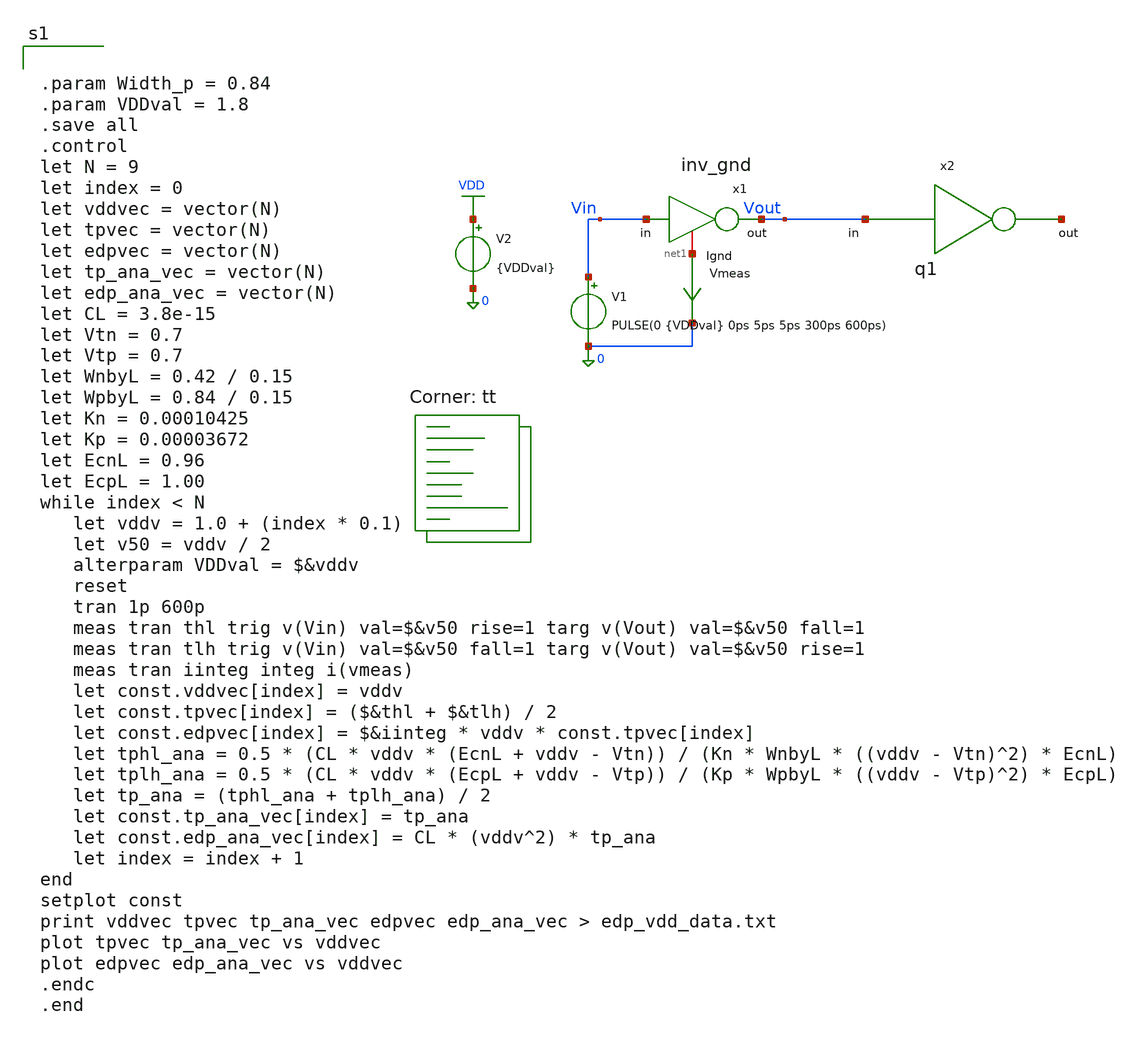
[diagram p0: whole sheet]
** sch_path: tutorial-3/source/qn_1_b.sch
**.subckt qn_1_b
V1 Vin 0 PULSE(0 {VDDval} 0ps 5ps 5ps 300ps 600ps)
V2 VDD 0 {VDDval}
x1 Vout Vin net1 inv_gnd
Vmeas net1 0 0
.save i(vmeas)
x2 net2 Vout q1
**** begin user architecture code


.param Width_p = 0.84
.param VDDval = 1.8
.save all
.control
let N = 9
let index = 0
let vddvec = vector(N)
let tpvec = vector(N)
let edpvec = vector(N)
let tp_ana_vec = vector(N)
let edp_ana_vec = vector(N)
let CL = 3.8e-15
let Vtn = 0.7
let Vtp = 0.7
let WnbyL = 0.42 / 0.15
let WpbyL = 0.84 / 0.15
let Kn = 0.00010425
let Kp = 0.00003672
let EcnL = 0.96
let EcpL = 1.00
while index < N
   let vddv = 1.0 + (index * 0.1)
   let v50 = vddv / 2
   alterparam VDDval = $&vddv
   reset
   tran 1p 600p
   meas tran thl trig v(Vin) val=$&v50 rise=1 targ v(Vout) val=$&v50 fall=1
   meas tran tlh trig v(Vin) val=$&v50 fall=1 targ v(Vout) val=$&v50 rise=1
   meas tran iinteg integ i(vmeas)
   let const.vddvec[index] = vddv
   let const.tpvec[index] = ($&thl + $&tlh) / 2
   let const.edpvec[index] = $&iinteg * vddv * const.tpvec[index]
   let tphl_ana = 0.5 * (CL * vddv * (EcnL + vddv - Vtn)) / (Kn * WnbyL * ((vddv - Vtn)^2) * EcnL)
   let tplh_ana = 0.5 * (CL * vddv * (EcpL + vddv - Vtp)) / (Kp * WpbyL * ((vddv - Vtp)^2) * EcpL)
   let tp_ana = (tphl_ana + tplh_ana) / 2
   let const.tp_ana_vec[index] = tp_ana
   let const.edp_ana_vec[index] = CL * (vddv^2) * tp_ana
   let index = index + 1
end
setplot const
print vddvec tpvec tp_ana_vec edpvec edp_ana_vec > edp_vdd_data.txt
plot tpvec tp_ana_vec vs vddvec
plot edpvec edp_ana_vec vs vddvec
.endc
.end

.lib $::SKYWATER_MODELS/sky130.lib.spice tt
**** end user architecture code
**.ends

* expanding   symbol:  inv_gnd.sym # of pins=3
** sym_path: tutorial-3/source/inv_gnd.sym
** sch_path: tutorial-3/source/inv_gnd.sch
.subckt inv_gnd out in Ignd
*.ipin in
*.opin out
*.iopin Ignd
XM1 out in Ignd GND sky130_fd_pr__nfet_01v8 L=0.15 W=0.42 nf=1 ad='int((nf+1)/2) * W/nf * 0.29' as='int((nf+2)/2) * W/nf * 0.29'
+ pd='2*int((nf+1)/2) * (W/nf + 0.29)' ps='2*int((nf+2)/2) * (W/nf + 0.29)' nrd='0.29 / W' nrs='0.29 / W'
+ sa=0 sb=0 sd=0 mult=1 m=1
XM2 out in VDD VDD sky130_fd_pr__pfet_01v8 L=0.15 W={width_p} nf=1 ad='int((nf+1)/2) * W/nf * 0.29' as='int((nf+2)/2) * W/nf * 0.29'
+ pd='2*int((nf+1)/2) * (W/nf + 0.29)' ps='2*int((nf+2)/2) * (W/nf + 0.29)' nrd='0.29 / W' nrs='0.29 / W'
+ sa=0 sb=0 sd=0 mult=1 m=1
.ends


* expanding   symbol:  q1.sym # of pins=2
** sym_path: tutorial-3/source/q1.sym
** sch_path: tutorial-3/source/q1.sch
.subckt q1 out in
*.ipin in
*.opin out
XM1 out in VDD VDD sky130_fd_pr__pfet_01v8 L=0.15 W={width_p} nf=1 ad='int((nf+1)/2) * W/nf * 0.29' as='int((nf+2)/2) * W/nf * 0.29'
+ pd='2*int((nf+1)/2) * (W/nf + 0.29)' ps='2*int((nf+2)/2) * (W/nf + 0.29)' nrd='0.29 / W' nrs='0.29 / W'
+ sa=0 sb=0 sd=0 mult=1 m=1
XM2 out in GND GND sky130_fd_pr__nfet_01v8 L=0.15 W=0.42 nf=1 ad='int((nf+1)/2) * W/nf * 0.29' as='int((nf+2)/2) * W/nf * 0.29'
+ pd='2*int((nf+1)/2) * (W/nf + 0.29)' ps='2*int((nf+2)/2) * (W/nf + 0.29)' nrd='0.29 / W' nrs='0.29 / W'
+ sa=0 sb=0 sd=0 mult=1 m=1
.ends

.GLOBAL VDD
.GLOBAL GND
.end
